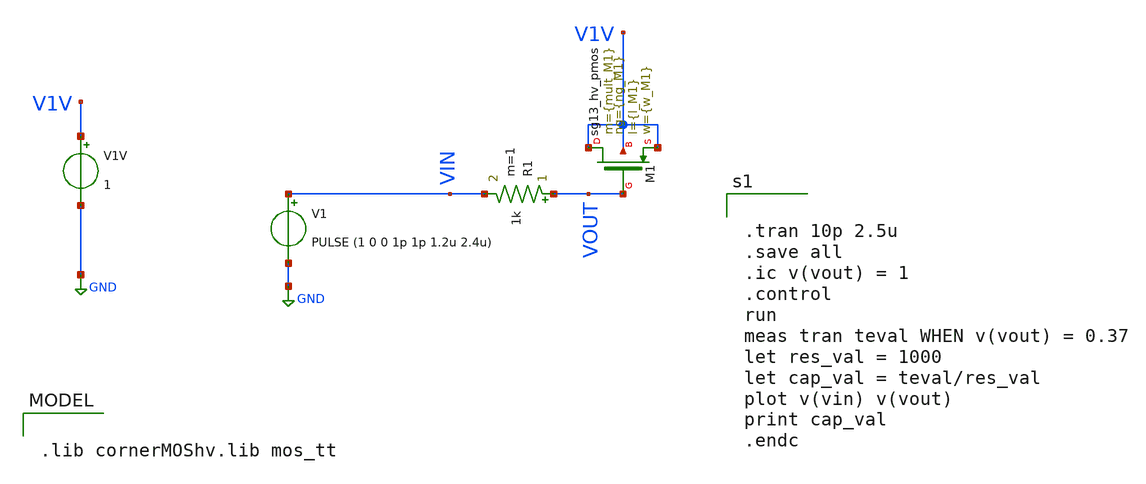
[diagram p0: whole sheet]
** sch_path: ChipUSM_AnalogTrack24/TestBenchs/TB_hvPMOS_cgate-ext.sch
**.subckt TB_hvPMOS_cgate-ext
R1 VOUT VIN 1k m=1
V1 VIN GND PULSE (1 0 0 1p 1p 1.2u 2.4u)
XM1 V1V VOUT V1V V1V sg13_hv_pmos w={w_M1} l={l_M1} ng={ng_M1} m={mult_M1} mm_ok=1
V1V V1V GND 1
**** begin user architecture code


.tran 10p 2.5u
.save all
.ic v(vout) = 1
.control
run
meas tran teval WHEN v(vout) = 0.37
let res_val = 1000
let cap_val = teval/res_val
plot v(vin) v(vout)
print cap_val
.endc




.param temp=27

.param mult_M1 = 12096
.param w_M1 =10u
*.param l_M1 =0.25u
.param l_M1 =0.4u
.param ng_M1 =1






.lib cornerMOShv.lib mos_tt

**** end user architecture code
**.ends
.GLOBAL GND
.end
